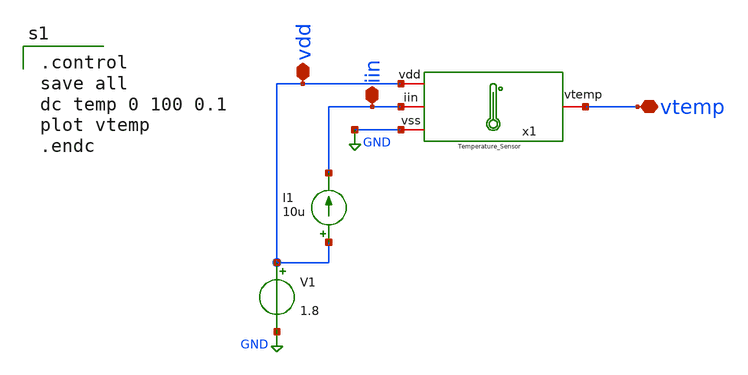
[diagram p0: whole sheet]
** sch_path: OTHER_SOLUTIONS_CONSIDERED/OTHER_BIAS_FOR_TEMPERATURE_SENSOR/TEMPERATURE_SENSOR/XSCHEM/Temp_Sensor_tb.sch
**.subckt Temp_Sensor_tb vdd vtemp iin
*.iopin vdd
*.iopin vtemp
*.iopin iin
V1 vdd GND 1.8
x1 vdd vtemp iin GND Temperature_Sensor
I1 vdd iin 10u
**** begin user architecture code

** opencircuitdesign pdks install
.lib $::SKYWATER_MODELS/sky130.lib.spice tt



.control
save all
dc temp 0 100 0.1
plot vtemp
.endc

**** end user architecture code
**.ends

* expanding   symbol:  Documentos/TESIS DE GRADO/WORK_IN_PROGRESS/My_xschem/Temperature_Sensor.sym #
*+ of pins=4
** sym_path: ANOTHER_SOLUTIONS_CONSIDERED/ANOTHER_BIAS_FOR_TEMPERATURE_SENSOR/TEMPERATURE_SENSOR/XSCHEM/Temperature_Sensor.sym
** sch_path: ANOTHER_SOLUTIONS_CONSIDERED/ANOTHER_BIAS_FOR_TEMPERATURE_SENSOR/TEMPERATURE_SENSOR/XSCHEM/Temperature_Sensor.sch
.subckt Temperature_Sensor vdd vtemp iin vss
*.iopin vdd
*.iopin vss
*.iopin vtemp
*.iopin iin
XM8 net1 vn net2 vss sky130_fd_pr__nfet_01v8_lvt L=2 W=20 nf=4 ad='int((nf+1)/2) * W/nf * 0.29' as='int((nf+2)/2) * W/nf * 0.29'
+ pd='2*int((nf+1)/2) * (W/nf + 0.29)' ps='2*int((nf+2)/2) * (W/nf + 0.29)' nrd='0.29 / W' nrs='0.29 / W'
+ sa=0 sb=0 sd=0 mult=1 m=1
XM9 vtemp vp net2 vss sky130_fd_pr__nfet_01v8_lvt L=0.5 W=20 nf=4 ad='int((nf+1)/2) * W/nf * 0.29' as='int((nf+2)/2) * W/nf * 0.29'
+ pd='2*int((nf+1)/2) * (W/nf + 0.29)' ps='2*int((nf+2)/2) * (W/nf + 0.29)' nrd='0.29 / W' nrs='0.29 / W'
+ sa=0 sb=0 sd=0 mult=1 m=1
XM10 net2 iin vss vss sky130_fd_pr__nfet_01v8 L=2 W=5 nf=1 ad='int((nf+1)/2) * W/nf * 0.29' as='int((nf+2)/2) * W/nf * 0.29'
+ pd='2*int((nf+1)/2) * (W/nf + 0.29)' ps='2*int((nf+2)/2) * (W/nf + 0.29)' nrd='0.29 / W' nrs='0.29 / W'
+ sa=0 sb=0 sd=0 mult=4 m=4
XM11 net1 net1 vdd vdd sky130_fd_pr__pfet_01v8_lvt L=2 W=5 nf=1 ad='int((nf+1)/2) * W/nf * 0.29' as='int((nf+2)/2) * W/nf * 0.29'
+ pd='2*int((nf+1)/2) * (W/nf + 0.29)' ps='2*int((nf+2)/2) * (W/nf + 0.29)' nrd='0.29 / W' nrs='0.29 / W'
+ sa=0 sb=0 sd=0 mult=4 m=4
XM12 vtemp net1 vdd vdd sky130_fd_pr__pfet_01v8_lvt L=2 W=5 nf=1 ad='int((nf+1)/2) * W/nf * 0.29' as='int((nf+2)/2) * W/nf * 0.29'
+ pd='2*int((nf+1)/2) * (W/nf + 0.29)' ps='2*int((nf+2)/2) * (W/nf + 0.29)' nrd='0.29 / W' nrs='0.29 / W'
+ sa=0 sb=0 sd=0 mult=4 m=4
XM13 net3 net3 vn vss sky130_fd_pr__nfet_01v8_lvt L=2 W=4 nf=1 ad='int((nf+1)/2) * W/nf * 0.29' as='int((nf+2)/2) * W/nf * 0.29'
+ pd='2*int((nf+1)/2) * (W/nf + 0.29)' ps='2*int((nf+2)/2) * (W/nf + 0.29)' nrd='0.29 / W' nrs='0.29 / W'
+ sa=0 sb=0 sd=0 mult=1 m=1
XQ3 vss vss vn sky130_fd_pr__pnp_05v5_W3p40L3p40 m=1
XM14 vdd net3 vp vss sky130_fd_pr__nfet_01v8_lvt L=2 W=4 nf=1 ad='int((nf+1)/2) * W/nf * 0.29' as='int((nf+2)/2) * W/nf * 0.29'
+ pd='2*int((nf+1)/2) * (W/nf + 0.29)' ps='2*int((nf+2)/2) * (W/nf + 0.29)' nrd='0.29 / W' nrs='0.29 / W'
+ sa=0 sb=0 sd=0 mult=10 m=10
XQ4 vss vss vp sky130_fd_pr__pnp_05v5_W3p40L3p40 m=1
XM15 iin iin vss vss sky130_fd_pr__nfet_01v8_lvt L=2 W=4 nf=1 ad='int((nf+1)/2) * W/nf * 0.29' as='int((nf+2)/2) * W/nf * 0.29'
+ pd='2*int((nf+1)/2) * (W/nf + 0.29)' ps='2*int((nf+2)/2) * (W/nf + 0.29)' nrd='0.29 / W' nrs='0.29 / W'
+ sa=0 sb=0 sd=0 mult=1 m=1
XM16 net4 iin vss vss sky130_fd_pr__nfet_01v8_lvt L=2 W=4 nf=1 ad='int((nf+1)/2) * W/nf * 0.29' as='int((nf+2)/2) * W/nf * 0.29'
+ pd='2*int((nf+1)/2) * (W/nf + 0.29)' ps='2*int((nf+2)/2) * (W/nf + 0.29)' nrd='0.29 / W' nrs='0.29 / W'
+ sa=0 sb=0 sd=0 mult=1 m=1
XM17 net4 net4 vdd vdd sky130_fd_pr__pfet_01v8_lvt L=2 W=4 nf=1 ad='int((nf+1)/2) * W/nf * 0.29' as='int((nf+2)/2) * W/nf * 0.29'
+ pd='2*int((nf+1)/2) * (W/nf + 0.29)' ps='2*int((nf+2)/2) * (W/nf + 0.29)' nrd='0.29 / W' nrs='0.29 / W'
+ sa=0 sb=0 sd=0 mult=1 m=1
XM18 net3 net4 vdd vdd sky130_fd_pr__pfet_01v8_lvt L=2 W=4 nf=1 ad='int((nf+1)/2) * W/nf * 0.29' as='int((nf+2)/2) * W/nf * 0.29'
+ pd='2*int((nf+1)/2) * (W/nf + 0.29)' ps='2*int((nf+2)/2) * (W/nf + 0.29)' nrd='0.29 / W' nrs='0.29 / W'
+ sa=0 sb=0 sd=0 mult=1 m=1
.ends

.GLOBAL GND
.end
